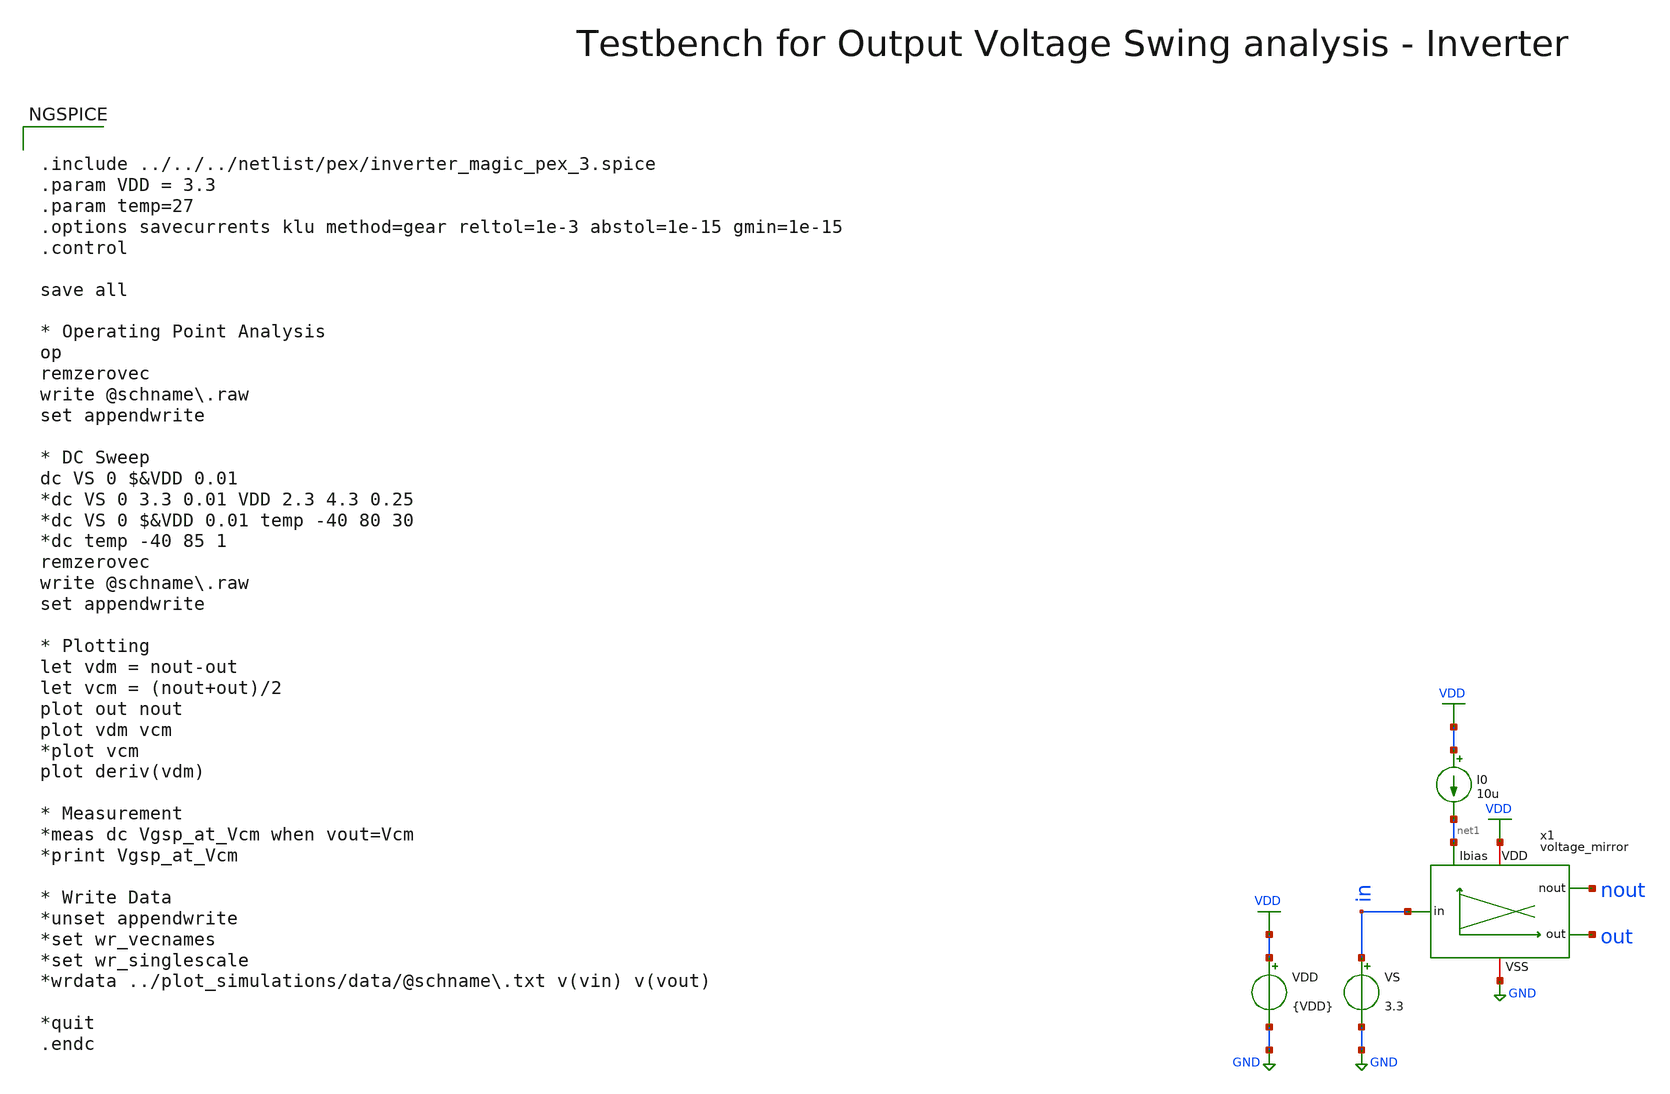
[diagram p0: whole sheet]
** sch_path: macros/heichips26_vcr/macros/switched_capacitor/testbenches/xschem/tb_voltage_mirror_dc.sch
**.subckt tb_voltage_mirror_dc
VDD VDD GND {VDD}
VS in GND 3.3
I0 VDD net1 10u
x1 net1 nout VDD in GND out voltage_mirror
**** begin user architecture code


.include ../../../netlist/pex/inverter_magic_pex_3.spice
.param VDD = 3.3
.param temp=27
.options savecurrents klu method=gear reltol=1e-3 abstol=1e-15 gmin=1e-15
.control

save all

* Operating Point Analysis
op
remzerovec
write @schname\.raw
set appendwrite

* DC Sweep
dc VS 0 $&VDD 0.01
*dc VS 0 3.3 0.01 VDD 2.3 4.3 0.25
*dc VS 0 $&VDD 0.01 temp -40 80 30
*dc temp -40 85 1
remzerovec
write @schname\.raw
set appendwrite

* Plotting
let vdm = nout-out
let vcm = (nout+out)/2
plot out nout
plot vdm vcm
*plot vcm
plot deriv(vdm)

* Measurement
*meas dc Vgsp_at_Vcm when vout=Vcm
*print Vgsp_at_Vcm

* Write Data
*unset appendwrite
*set wr_vecnames
*set wr_singlescale
*wrdata ../plot_simulations/data/@schname\.txt v(vin) v(vout)

*quit
.endc



.lib cornerMOSlv.lib mos_tt
.lib cornerMOShv.lib mos_tt
.lib cornerRES.lib res_typ
.lib cornerDIO.lib dio_tt

**** end user architecture code
**.ends

* expanding   symbol:  voltage_mirror.sym # of pins=6
** sym_path: macros/heichips26_vcr/macros/switched_capacitor/schematic/xschem/voltage_mirror.sym
** sch_path: macros/heichips26_vcr/macros/switched_capacitor/schematic/xschem/voltage_mirror.sch
.subckt voltage_mirror Ibias nout VDD in VSS out
*.iopin VDD
*.iopin VSS
*.ipin in
*.opin out
*.opin nout
*.ipin Ibias
**** begin user architecture code


.param n_w = 6u
.param n_l = 5u
.param p_w = 10u
.param p_l = 2u


**** end user architecture code
XM1 Ibias Ibias VSS VSS sg13_hv_nmos w=1.9*n_w l=n_l ng=2 m=1 mm_ok=1
XR1 in Ibias GND rhigh w=0.5e-6 l=34e-6 m=1 b=0 mm_ok=1
XM2 net1 net1 VDD VDD sg13_hv_pmos w=p_w l=p_l ng=1 m=1 mm_ok=1
XM3 nout Ibias VSS VSS sg13_hv_nmos w=n_w l=n_l ng=1 m=1 mm_ok=1
XM4 out net1 VDD VDD sg13_hv_pmos w=p_w l=p_l ng=1 m=1 mm_ok=1
XM5 net1 Ibias VSS VSS sg13_hv_nmos w=n_w l=n_l ng=1 m=1 mm_ok=1
XR2 VDD nout GND rhigh w=0.5e-6 l=34e-6 m=1 b=0 mm_ok=1
XR3 out VSS GND rhigh w=0.5e-6 l=34e-6 m=1 b=0 mm_ok=1
.ends

.GLOBAL GND
.GLOBAL VDD
.end
